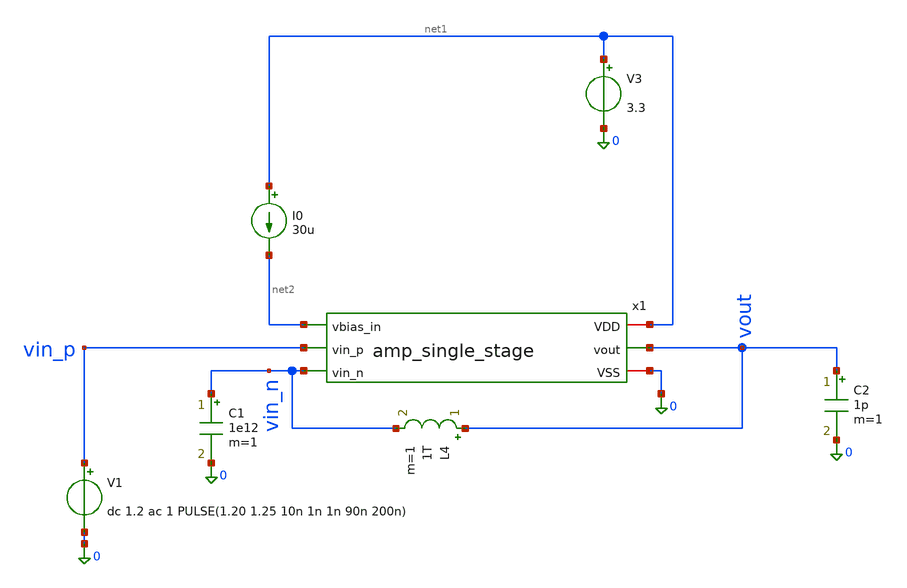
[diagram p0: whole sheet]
** sch_path: xschem/tb_amp_single_stg_ac.sch
**.subckt tb_amp_single_stg_ac
C2 vout 0 1p m=1
V3 net1 0 3.3
V1 vin_p 0 dc 1.2 ac 1 PULSE(1.20 1.25 10n 1n 1n 90n 200n)
L4 vout vin_n 1T m=1
C1 vin_n 0 1e12 m=1
x1 net1 net2 vout 0 vin_p vin_n amp_single_stage
I0 net1 net2 30u
**** begin user architecture code


* GF180MCU Global Process & Noise Parameters (Must be before .lib)
.param fnoicor = 0
.param sw_stat_global = 0
.param sw_stat_mismatch = 1

* PDK Model Include (MOSFETs)
.lib /foss/pdks/ciel/gf180mcu/versions/026824c7969ce6f4fc9678e6ca04b0a06a596c4b/gf180mcuD/libs.tech/ngspice/sm141064.ngspice typical

* MIM Capacitor Model (bypasses missing OSDI library)
.subckt cap_mim_2f0ff c0 c1 c_width=1e-6 c_length=1e-6
C_mim c0 c1 2.5p
.ends cap_mim_2f0ff

* Remove any .ac or .tran lines outside .control so they don't run prematurely
.save all

.control
destroy all

* ======================================================================
* 1. DC OPERATING POINT & TRANSISTOR SATURATION CHECK
* ======================================================================
op

let v_inp_dc   = v(vin_p)
let v_inn_dc   = v(vin_n)
let v_out_dc   = v(vout)
let v_diode_dc = v(x1.x2.net3)
let i_vdd_ua   = abs(v3#branch) * 1e6
let p_total_mw = i_vdd_ua * 3.3 / 1e3

echo ======================================================================
echo                    1. DC OPERATING VOLTAGES & POWER
echo ======================================================================
print v_inp_dc v_inn_dc v_out_dc v_diode_dc
print i_vdd_ua p_total_mw

* ======================================================================
* 2. AUTOMATED TRANSISTOR SATURATION CHECKER
* ======================================================================
* Calculates margin = abs(VDS) - abs(VDSAT).
* Margin negative -> TRIODE / LINEAR (Failing)
* 0 to 50mV -> EDGE OF SATURATION (Warning)

let thr = 0.05

* --- Calculate Margins for Stage 1 (x1.x2) ---
let m_s1_xm1  = abs(@m.x1.x2.xm1.m0[vds])  - abs(@m.x1.x2.xm1.m0[vdsat])
let m_s1_xm2  = abs(@m.x1.x2.xm2.m0[vds])  - abs(@m.x1.x2.xm2.m0[vdsat])
let m_s1_xm3  = abs(@m.x1.x2.xm3.m0[vds])  - abs(@m.x1.x2.xm3.m0[vdsat])
let m_s1_xm4  = abs(@m.x1.x2.xm4.m0[vds])  - abs(@m.x1.x2.xm4.m0[vdsat])
let m_s1_xm5  = abs(@m.x1.x2.xm5.m0[vds])  - abs(@m.x1.x2.xm5.m0[vdsat])
let m_s1_xm7  = abs(@m.x1.x2.xm7.m0[vds])  - abs(@m.x1.x2.xm7.m0[vdsat])
let m_s1_xm8  = abs(@m.x1.x2.xm8.m0[vds])  - abs(@m.x1.x2.xm8.m0[vdsat])
let m_s1_xm9  = abs(@m.x1.x2.xm9.m0[vds])  - abs(@m.x1.x2.xm9.m0[vdsat])
let m_s1_xm10 = abs(@m.x1.x2.xm10.m0[vds]) - abs(@m.x1.x2.xm10.m0[vdsat])

* --- Calculate Margins for Bias Generator (x1.x1) ---
let m_bg_xm1  = abs(@m.x1.x1.xm1.m0[vds])  - abs(@m.x1.x1.xm1.m0[vdsat])
let m_bg_xm3  = abs(@m.x1.x1.xm3.m0[vds])  - abs(@m.x1.x1.xm3.m0[vdsat])
let m_bg_xm4  = abs(@m.x1.x1.xm4.m0[vds])  - abs(@m.x1.x1.xm4.m0[vdsat])
let m_bg_xm5  = abs(@m.x1.x1.xm5.m0[vds])  - abs(@m.x1.x1.xm5.m0[vdsat])
let m_bg_xm6  = abs(@m.x1.x1.xm6.m0[vds])  - abs(@m.x1.x1.xm6.m0[vdsat])
let m_bg_xm7  = abs(@m.x1.x1.xm7.m0[vds])  - abs(@m.x1.x1.xm7.m0[vdsat])
let m_bg_xm8  = abs(@m.x1.x1.xm8.m0[vds])  - abs(@m.x1.x1.xm8.m0[vdsat])
let m_bg_xm9  = abs(@m.x1.x1.xm9.m0[vds])  - abs(@m.x1.x1.xm9.m0[vdsat])

echo ======================================================================
echo                  *** TRIODE WARNINGS - MARGIN NEGATIVE ***
echo ======================================================================
if m_s1_xm1 < 0
  echo Stage 1 XM1 NMOS Input Right     : $&m_s1_xm1 V
end
if m_s1_xm2 < 0
  echo Stage 1 XM2 PMOS Cascode Left    : $&m_s1_xm2 V
end
if m_s1_xm3 < 0
  echo Stage 1 XM3 NMOS Tail            : $&m_s1_xm3 V
end
if m_s1_xm4 < 0
  echo Stage 1 XM4 NMOS Cascode Right   : $&m_s1_xm4 V
end
if m_s1_xm5 < 0
  echo Stage 1 XM5 NMOS Cascode Left    : $&m_s1_xm5 V
end
if m_s1_xm7 < 0
  echo Stage 1 XM7 NMOS Input Left      : $&m_s1_xm7 V
end
if m_s1_xm8 < 0
  echo Stage 1 XM8 PMOS Cascode Right   : $&m_s1_xm8 V
end
if m_s1_xm9 < 0
  echo Stage 1 XM9 PMOS Mirror Left     : $&m_s1_xm9 V
end
if m_s1_xm10 < 0
  echo Stage 1 XM10 PMOS Mirror Right   : $&m_s1_xm10 V
end
if m_bg_xm1 < 0
  echo Bias XM1 NMOS Ref Diode          : $&m_bg_xm1 V
end
if m_bg_xm3 < 0
  echo Bias XM3 NMOS Mirror             : $&m_bg_xm3 V
end
if m_bg_xm4 < 0
  echo Bias XM4 PMOS Mirror             : $&m_bg_xm4 V
end
if m_bg_xm5 < 0
  echo Bias XM5 PMOS Mirror             : $&m_bg_xm5 V
end
if m_bg_xm6 < 0
  echo Bias XM6 NMOS Mirror             : $&m_bg_xm6 V
end
if m_bg_xm7 < 0
  echo Bias XM7 NMOS Mirror             : $&m_bg_xm7 V
end
if m_bg_xm8 < 0
  echo Bias XM8 NMOS Cascode Bias Gen   : $&m_bg_xm8 V
end
if m_bg_xm9 < 0
  echo Bias XM9 PMOS Cascode Bias Gen   : $&m_bg_xm9 V
end

echo .
echo ======================================================================
echo             *** EDGE OF SATURATION - MARGIN 0 TO 50mV ***
echo ======================================================================
if m_s1_xm1 > 0
  if m_s1_xm1 < thr
    echo Stage 1 XM1 NMOS Input Right     : $&m_s1_xm1 V
  end
end
if m_s1_xm2 > 0
  if m_s1_xm2 < thr
    echo Stage 1 XM2 PMOS Cascode Left    : $&m_s1_xm2 V
  end
end
if m_s1_xm3 > 0
  if m_s1_xm3 < thr
    echo Stage 1 XM3 NMOS Tail            : $&m_s1_xm3 V
  end
end
if m_s1_xm4 > 0
  if m_s1_xm4 < thr
    echo Stage 1 XM4 NMOS Cascode Right   : $&m_s1_xm4 V
  end
end
if m_s1_xm5 > 0
  if m_s1_xm5 < thr
    echo Stage 1 XM5 NMOS Cascode Left    : $&m_s1_xm5 V
  end
end
if m_s1_xm7 > 0
  if m_s1_xm7 < thr
    echo Stage 1 XM7 NMOS Input Left      : $&m_s1_xm7 V
  end
end
if m_s1_xm8 > 0
  if m_s1_xm8 < thr
    echo Stage 1 XM8 PMOS Cascode Right   : $&m_s1_xm8 V
  end
end
if m_s1_xm9 > 0
  if m_s1_xm9 < thr
    echo Stage 1 XM9 PMOS Mirror Left     : $&m_s1_xm9 V
  end
end
if m_s1_xm10 > 0
  if m_s1_xm10 < thr
    echo Stage 1 XM10 PMOS Mirror Right   : $&m_s1_xm10 V
  end
end
if m_bg_xm1 > 0
  if m_bg_xm1 < thr
    echo Bias XM1 NMOS Ref Diode          : $&m_bg_xm1 V
  end
end
if m_bg_xm3 > 0
  if m_bg_xm3 < thr
    echo Bias XM3 NMOS Mirror             : $&m_bg_xm3 V
  end
end
if m_bg_xm4 > 0
  if m_bg_xm4 < thr
    echo Bias XM4 PMOS Mirror             : $&m_bg_xm4 V
  end
end
if m_bg_xm5 > 0
  if m_bg_xm5 < thr
    echo Bias XM5 PMOS Mirror             : $&m_bg_xm5 V
  end
end
if m_bg_xm6 > 0
  if m_bg_xm6 < thr
    echo Bias XM6 NMOS Mirror             : $&m_bg_xm6 V
  end
end
if m_bg_xm7 > 0
  if m_bg_xm7 < thr
    echo Bias XM7 NMOS Mirror             : $&m_bg_xm7 V
  end
end
if m_bg_xm8 > 0
  if m_bg_xm8 < thr
    echo Bias XM8 NMOS Cascode Bias Gen   : $&m_bg_xm8 V
  end
end
if m_bg_xm9 > 0
  if m_bg_xm9 < thr
    echo Bias XM9 PMOS Cascode Bias Gen   : $&m_bg_xm9 V
  end
end

* ======================================================================
* 3. AC FREQUENCY RESPONSE (OPEN-LOOP: L4=1e12, C1=1e12)
* ======================================================================
alter l4 = 1e12
alter c1 = 1e12
ac dec 35 1 5G

let v_out_ac  = v(vout)
let gain_db   = db(v_out_ac)
let phase_deg = cph(v_out_ac) * 180 / 3.1415926535

meas ac dc_gain find gain_db at=1
let g_3db = dc_gain - 3
meas ac f_3db when gain_db = g_3db
meas ac f_ugbw when gain_db = 0
meas ac ph_ugbw find phase_deg when gain_db = 0
let pm = 180 + ph_ugbw

echo ======================================================================
echo                    3. AC FREQUENCY RESPONSE RESULTS
echo ======================================================================
print dc_gain
print f_3db
print f_ugbw
print pm

* ======================================================================
* 4. TRANSIENT & SLEW RATE (CLOSED-LOOP UNITY-GAIN: L4=1p, C1=1f)
* ======================================================================
alter l4 = 1e-12
alter c1 = 1e-18
tran 0.1n 1000n

meas tran v_init find v(vout) at=9n
meas tran v_max MAX v(vout) from=10n to=100n
meas tran v_min MIN v(vout) from=100n to=200n

* 20% to 80% levels (1.21V to 1.24V) with from=10n to ignore startup settling
meas tran t_rise TRIG v(vout) VAL=1.21 RISE=1 TARG v(vout) VAL=1.24 RISE=1 from=10n
meas tran t_fall TRIG v(vout) VAL=1.24 FALL=1 TARG v(vout) VAL=1.21 FALL=1 from=50n

* Calculate Slew Rates
let sr_rise_v_us = (0.03 / t_rise) / 1e6
let sr_fall_v_us = (0.03 / t_fall) / 1e6

echo ======================================================================
echo                    4. TRANSIENT & SLEW RATE RESULTS
echo ======================================================================
print v_init v_max v_min
print t_rise sr_rise_v_us
print t_fall sr_fall_v_us
* ======================================================================
* 5. DC SWEEP (OUTPUT SWING & ICMR)
* ======================================================================
alter l4 = 1e-12
alter c1 = 1e-18
dc v1 0 3.3 1m

* Calculate Output Swing
let vout_deriv = deriv(v(vout))
meas dc swing_min find v(vout) when vout_deriv=0.9 cross=1
meas dc swing_max find v(vout) when vout_deriv=0.9 cross=last
let total_swing = swing_max - swing_min

* Calculate ICMR Margins using node voltages to bypass ngspice vector bugs
* VTH is approx 0.45V for the GF180 3.3V NMOS devices
let vds_tail_sweep = v(x1.x2.net6)
let vdsat_tail_sweep = v(x1.net1) - 0.45
let marg_tail_sweep = vds_tail_sweep - vdsat_tail_sweep

let vds_in_sweep = v(x1.x2.net4) - v(x1.x2.net6)
let vgs_in_sweep = v(vin_n) - v(x1.x2.net6)
let vdsat_in_sweep = vgs_in_sweep - 0.45
let marg_in_sweep = vds_in_sweep - vdsat_in_sweep

echo ======================================================================
echo                    5. OUTPUT SWING RESULTS
echo ======================================================================
print swing_min swing_max total_swing

* ======================================================================
* 6. NOISE ANALYSIS
* ======================================================================
noise v(vout) v1 dec 35 1 5G

echo ======================================================================
echo                    6. NOISE ANALYSIS RESULTS
echo ======================================================================
print inoise_total onoise_total

* ======================================================================
* 7. PLOTS
* ======================================================================
setplot ac1
plot db(v(vout)) title 'Open-Loop Gain (dB)'
plot (cph(v(vout))*180/3.14159265) title 'Open-Loop Phase (Deg)'

setplot tran1
plot v(vout) v(vin_p) title 'Closed-Loop Transient Step Response'

setplot dc1
plot v(vout) v(vin_p) title 'DC Transfer Characteristic (Output Swing)'
*plot marg_tail_sweep marg_in_sweep title 'ICMR: Saturation Margins (>0 is good)'

*setplot noise1
*plot inoise_spectrum title 'Input-Referred Noise Spectrum (V/rtHz)'

.endc


**** end user architecture code
**.ends

* expanding   symbol:  ttgf-ece298-analog-op-amp/xschem/amp_single_stage.sym # of pins=6
** sym_path: xschem/amp_single_stage.sym
** sch_path: xschem/amp_single_stage.sch
.subckt amp_single_stage VDD vbias_in vout VSS vin_p vin_n
*.opin vout
*.ipin vin_n
*.ipin vin_p
*.iopin VSS
*.iopin VDD
*.ipin vbias_in
x1 VDD vbias_in net1 net2 VSS amp_bias
x2 VDD vout net1 net2 vin_n vin_p vbias_in VSS amp_stg_1
.ends


* expanding   symbol:  ttgf-ece298-analog-op-amp/xschem/amp_bias.sym # of pins=5
** sym_path: xschem/amp_bias.sym
** sch_path: xschem/amp_bias.sch
.subckt amp_bias VDD vbias_in vbias_1 vbias_2 VSS
*.iopin VDD
*.iopin VSS
*.opin vbias_1
*.opin vbias_2
*.ipin vbias_in
XM1 vbias_in vbias_in VSS VSS nfet_03v3 L=1.4u W=32u nf=4 ad='int((nf+1)/2) * W/nf * 0.18u' as='int((nf+2)/2)
+ * W/nf * 0.18u' pd='2*int((nf+1)/2) * (W/nf + 0.18u)' ps='2*int((nf+2)/2) * (W/nf + 0.18u)' nrd='0.18u
+ / W' nrs='0.18u / W' sa=0 sb=0 sd=0 m=1 par=1
XM3 net1 vbias_in VSS VSS nfet_03v3 L=1.4u W=8u nf=1 ad='int((nf+1)/2) * W/nf * 0.18u' as='int((nf+2)/2)
+ * W/nf * 0.18u' pd='2*int((nf+1)/2) * (W/nf + 0.18u)' ps='2*int((nf+2)/2) * (W/nf + 0.18u)' nrd='0.18u
+ / W' nrs='0.18u / W' sa=0 sb=0 sd=0 m=1 par=1
XM4 net1 net1 VDD VDD pfet_03v3 L=1.4u W=8u nf=1 ad='int((nf+1)/2) * W/nf * 0.18u' as='int((nf+2)/2)
+ * W/nf * 0.18u' pd='2*int((nf+1)/2) * (W/nf + 0.18u)' ps='2*int((nf+2)/2) * (W/nf + 0.18u)' nrd='0.18u
+ / W' nrs='0.18u / W' sa=0 sb=0 sd=0 m=1
XM5 vbias_2 net1 VDD VDD pfet_03v3 L=1.4u W=8u nf=1 ad='int((nf+1)/2) * W/nf * 0.18u' as='int((nf+2)/2)
+ * W/nf * 0.18u' pd='2*int((nf+1)/2) * (W/nf + 0.18u)' ps='2*int((nf+2)/2) * (W/nf + 0.18u)' nrd='0.18u
+ / W' nrs='0.18u / W' sa=0 sb=0 sd=0 m=1
XM6 vbias_1 vbias_in VSS VSS nfet_03v3 L=1.4u W=8u nf=1 ad='int((nf+1)/2) * W/nf * 0.18u' as='int((nf+2)/2)
+ * W/nf * 0.18u' pd='2*int((nf+1)/2) * (W/nf + 0.18u)' ps='2*int((nf+2)/2) * (W/nf + 0.18u)' nrd='0.18u
+ / W' nrs='0.18u / W' sa=0 sb=0 sd=0 m=1 par=1
XM7 net2 net2 VSS VSS nfet_03v3 L=1.4u W=6u nf=1 ad='int((nf+1)/2) * W/nf * 0.18u' as='int((nf+2)/2)
+ * W/nf * 0.18u' pd='2*int((nf+1)/2) * (W/nf + 0.18u)' ps='2*int((nf+2)/2) * (W/nf + 0.18u)' nrd='0.18u
+ / W' nrs='0.18u / W' sa=0 sb=0 sd=0 m=1 par=1
XM8 vbias_2 vbias_2 net2 VSS nfet_03v3 L=1.4u W=6u nf=1 ad='int((nf+1)/2) * W/nf * 0.18u' as='int((nf+2)/2)
+ * W/nf * 0.18u' pd='2*int((nf+1)/2) * (W/nf + 0.18u)' ps='2*int((nf+2)/2) * (W/nf + 0.18u)' nrd='0.18u
+ / W' nrs='0.18u / W' sa=0 sb=0 sd=0 m=1 par=1
XM9 vbias_1 vbias_1 VDD VDD pfet_03v3 L=1.4u W=1u nf=1 ad='int((nf+1)/2) * W/nf * 0.18u' as='int((nf+2)/2)
+ * W/nf * 0.18u' pd='2*int((nf+1)/2) * (W/nf + 0.18u)' ps='2*int((nf+2)/2) * (W/nf + 0.18u)' nrd='0.18u
+ / W' nrs='0.18u / W' sa=0 sb=0 sd=0 m=1
.ends


* expanding   symbol:  ttgf-ece298-analog-op-amp/xschem/amp_stg_1.sym # of pins=8
** sym_path: xschem/amp_stg_1.sym
** sch_path: xschem/amp_stg_1.sch
.subckt amp_stg_1 VDD vout vbias_1 vbias_2 vn vp vbias_tail VSS
*.iopin VDD
*.iopin VSS
*.ipin vn
*.ipin vp
*.opin vout
*.ipin vbias_tail
*.ipin vbias_2
*.ipin vbias_1
XM2 net3 vbias_1 net1 VDD pfet_03v3 L=2.0u W=28u nf=4 ad='int((nf+1)/2) * W/nf * 0.18u' as='int((nf+2)/2)
+ * W/nf * 0.18u' pd='2*int((nf+1)/2) * (W/nf + 0.18u)' ps='2*int((nf+2)/2) * (W/nf + 0.18u)' nrd='0.18u
+ / W' nrs='0.18u / W' sa=0 sb=0 sd=0 m=1 par=1
XM1 net4 vn net6 VSS nfet_03v3 L=1.4u W=16u nf=2 ad='int((nf+1)/2) * W/nf * 0.18u' as='int((nf+2)/2)
+ * W/nf * 0.18u' pd='2*int((nf+1)/2) * (W/nf + 0.18u)' ps='2*int((nf+2)/2) * (W/nf + 0.18u)' nrd='0.18u
+ / W' nrs='0.18u / W' sa=0 sb=0 sd=0 m=2 par=2
XM3 net6 vbias_tail VSS VSS nfet_03v3 L=1.4u W=32u nf=4 ad='int((nf+1)/2) * W/nf * 0.18u' as='int((nf+2)/2)
+ * W/nf * 0.18u' pd='2*int((nf+1)/2) * (W/nf + 0.18u)' ps='2*int((nf+2)/2) * (W/nf + 0.18u)' nrd='0.18u
+ / W' nrs='0.18u / W' sa=0 sb=0 sd=0 m=1 par=1
XM4 vout vbias_2 net4 VSS nfet_03v3 L=2.0u W=16u nf=4 ad='int((nf+1)/2) * W/nf * 0.18u' as='int((nf+2)/2)
+ * W/nf * 0.18u' pd='2*int((nf+1)/2) * (W/nf + 0.18u)' ps='2*int((nf+2)/2) * (W/nf + 0.18u)' nrd='0.18u
+ / W' nrs='0.18u / W' sa=0 sb=0 sd=0 m=1 par=1
XM5 net3 vbias_2 net5 VSS nfet_03v3 L=2.0u W=16u nf=4 ad='int((nf+1)/2) * W/nf * 0.18u' as='int((nf+2)/2)
+ * W/nf * 0.18u' pd='2*int((nf+1)/2) * (W/nf + 0.18u)' ps='2*int((nf+2)/2) * (W/nf + 0.18u)' nrd='0.18u
+ / W' nrs='0.18u / W' sa=0 sb=0 sd=0 m=1 par=1
XM7 net5 vp net6 VSS nfet_03v3 L=1.4u W=16u nf=2 ad='int((nf+1)/2) * W/nf * 0.18u' as='int((nf+2)/2)
+ * W/nf * 0.18u' pd='2*int((nf+1)/2) * (W/nf + 0.18u)' ps='2*int((nf+2)/2) * (W/nf + 0.18u)' nrd='0.18u
+ / W' nrs='0.18u / W' sa=0 sb=0 sd=0 m=2 par=2
XM8 vout vbias_1 net2 VDD pfet_03v3 L=2.0u W=28u nf=4 ad='int((nf+1)/2) * W/nf * 0.18u' as='int((nf+2)/2)
+ * W/nf * 0.18u' pd='2*int((nf+1)/2) * (W/nf + 0.18u)' ps='2*int((nf+2)/2) * (W/nf + 0.18u)' nrd='0.18u
+ / W' nrs='0.18u / W' sa=0 sb=0 sd=0 m=1 par=1
XM9 net1 net3 VDD VDD pfet_03v3 L=2.0u W=28u nf=4 ad='int((nf+1)/2) * W/nf * 0.18u' as='int((nf+2)/2)
+ * W/nf * 0.18u' pd='2*int((nf+1)/2) * (W/nf + 0.18u)' ps='2*int((nf+2)/2) * (W/nf + 0.18u)' nrd='0.18u
+ / W' nrs='0.18u / W' sa=0 sb=0 sd=0 m=1 par=1
XM10 net2 net3 VDD VDD pfet_03v3 L=2.0u W=28u nf=4 ad='int((nf+1)/2) * W/nf * 0.18u' as='int((nf+2)/2)
+ * W/nf * 0.18u' pd='2*int((nf+1)/2) * (W/nf + 0.18u)' ps='2*int((nf+2)/2) * (W/nf + 0.18u)' nrd='0.18u
+ / W' nrs='0.18u / W' sa=0 sb=0 sd=0 m=1 par=1
.ends

.end
